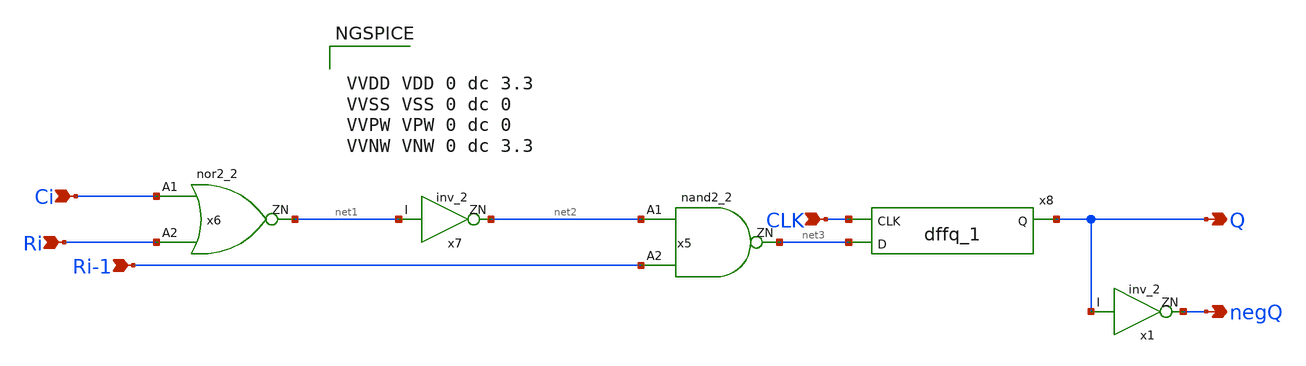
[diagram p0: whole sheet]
** sch_path: xschem/Local_encoder.sch
**.subckt Local_encoder Ri-1 Ri Ci CLK Q negQ
*.ipin Ri-1
*.ipin Ri
*.ipin Ci
*.ipin CLK
*.opin Q
*.opin negQ
x5 net2 Ri-1 net3 VDD VNW VPW VSS gf180mcu_fd_sc_mcu7t5v0__nand2_2
x6 Ci Ri net1 VDD VNW VPW VSS gf180mcu_fd_sc_mcu7t5v0__nor2_2
x7 net1 net2 VDD VNW VPW VSS gf180mcu_fd_sc_mcu7t5v0__inv_2
x8 CLK net3 VDD VNW VPW VSS gf180mcu_fd_sc_mcu7t5v0__dffq_1
x1 Q negQ VDD VNW VPW VSS gf180mcu_fd_sc_mcu7t5v0__inv_2
**** begin user architecture code


VVDD VDD 0 dc 3.3
VVSS VSS 0 dc 0
VVPW VPW 0 dc 0
VVNW VNW 0 dc 3.3


**** end user architecture code
**.ends
.end
